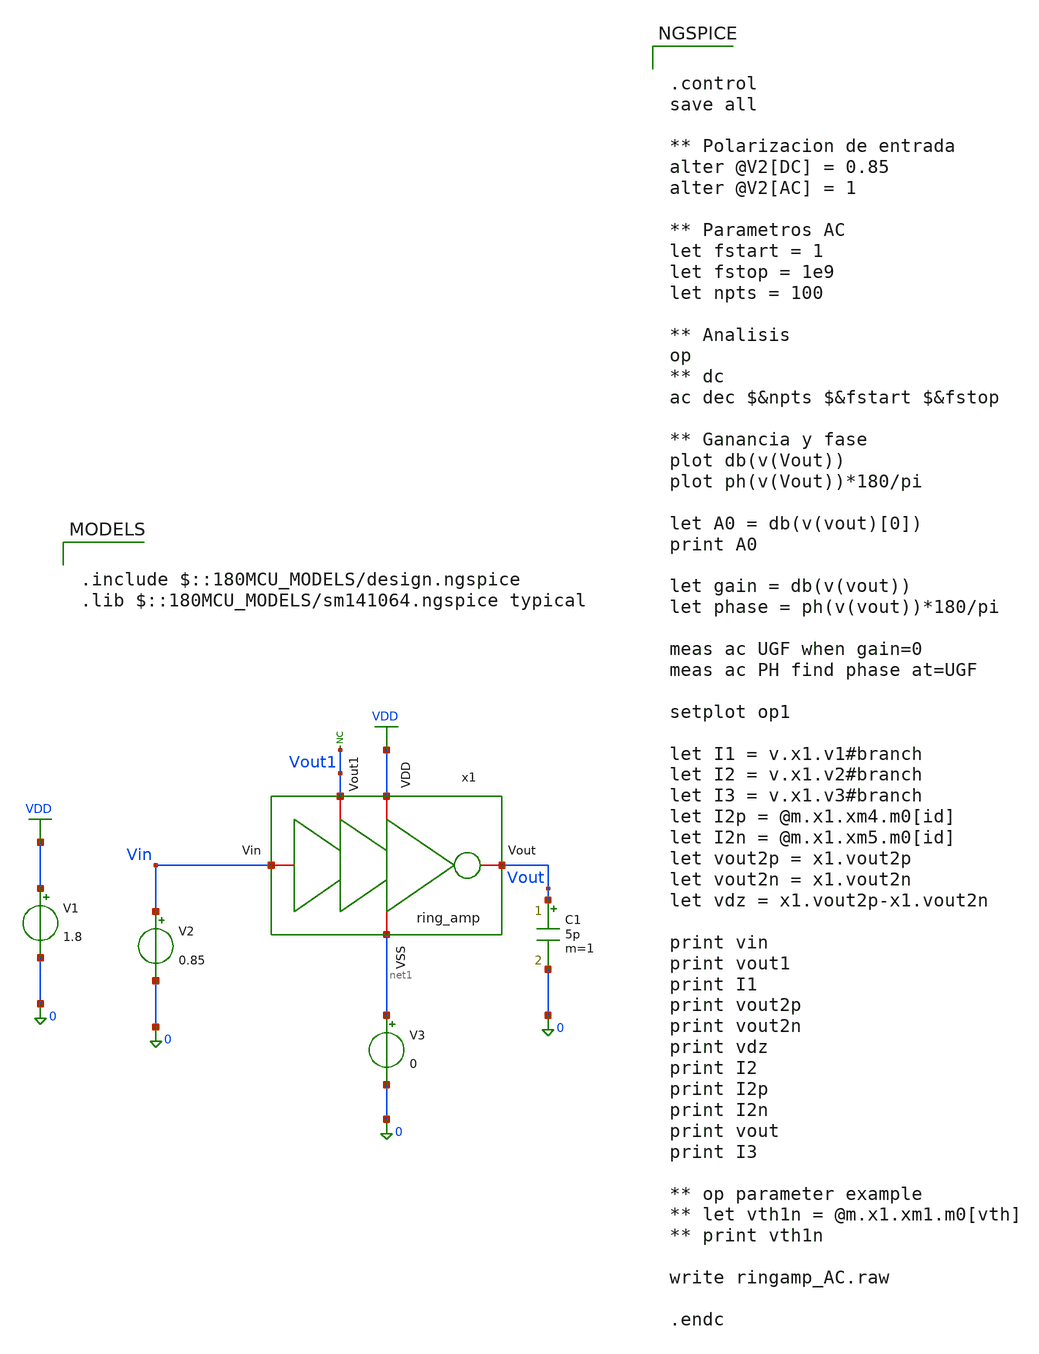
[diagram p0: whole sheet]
** sch_path: designs/DS_modulator/ring_amp/xschem/ring_amp_TB_AC.sch
**.subckt ring_amp_TB_AC
C1 Vout 0 5p m=1
V1 VDD 0 1.8
V2 Vin 0 0.85
x1 VDD Vin Vout Vout1 net1 ring_amp
V3 net1 0 0
* noconn Vout1
**** begin user architecture code

.include $::180MCU_MODELS/design.ngspice
.lib $::180MCU_MODELS/sm141064.ngspice typical



.control
save all

** Polarizacion de entrada
alter @V2[DC] = 0.85
alter @V2[AC] = 1

** Parametros AC
let fstart = 1
let fstop = 1e9
let npts = 100

** Analisis
op
** dc
ac dec $&npts $&fstart $&fstop

** Ganancia y fase
plot db(v(Vout))
plot ph(v(Vout))*180/pi

let A0 = db(v(vout)[0])
print A0

let gain = db(v(vout))
let phase = ph(v(vout))*180/pi

meas ac UGF when gain=0
meas ac PH find phase at=UGF

setplot op1

let I1 = v.x1.v1#branch
let I2 = v.x1.v2#branch
let I3 = v.x1.v3#branch
let I2p = @m.x1.xm4.m0[id]
let I2n = @m.x1.xm5.m0[id]
let vout2p = x1.vout2p
let vout2n = x1.vout2n
let vdz = x1.vout2p-x1.vout2n

print vin
print vout1
print I1
print vout2p
print vout2n
print vdz
print I2
print I2p
print I2n
print vout
print I3

** op parameter example
** let vth1n = @m.x1.xm1.m0[vth]
** print vth1n

write ringamp_AC.raw

.endc


**** end user architecture code
**.ends
.GLOBAL VDD
.end
